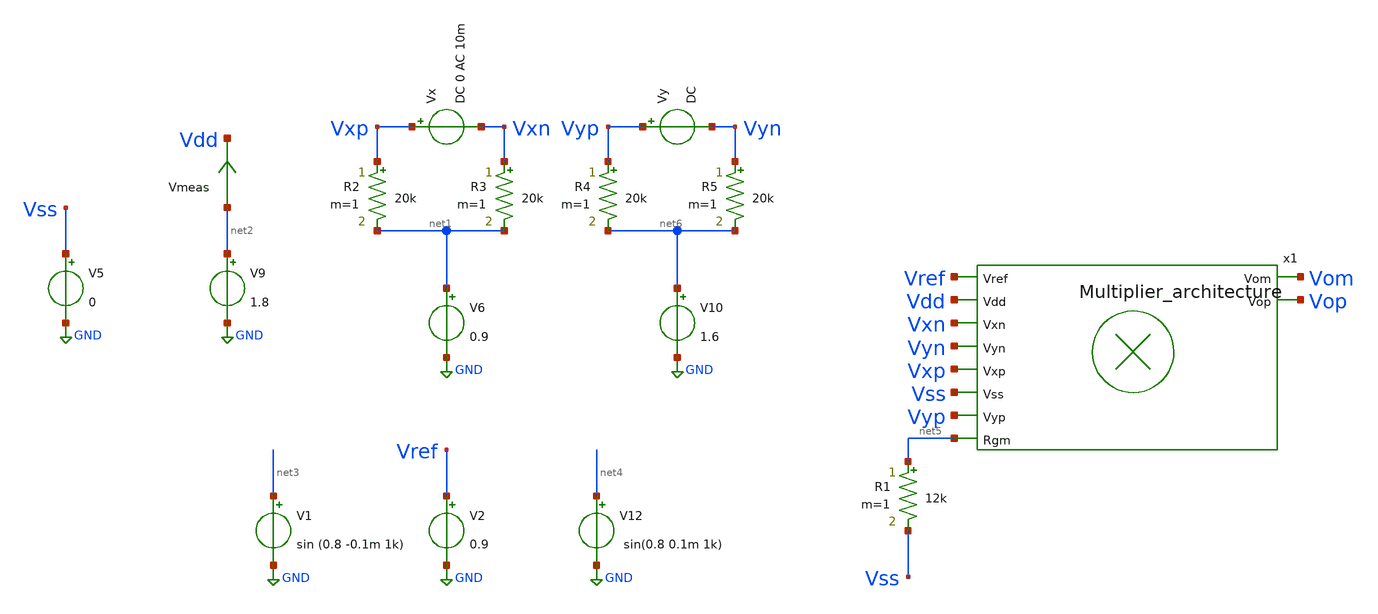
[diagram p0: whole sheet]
** sch_path: src/Multiplier/testbenches/Multiplier_tb.sch
**.subckt Multiplier_tb
x1 Vref Vom Vdd Vxn Vyn Vxp Vss Vyp Vop net5 Multiplier_architecture
Vx Vxp Vxn DC 0 AC 10m
V6 net1 GND 0.9
V9 net2 GND 1.8
Vmeas net2 Vdd 0
.save i(vmeas)
V1 net3 GND sin (0.8 -0.1m 1k)
V12 net4 GND sin(0.8 0.1m 1k)
V5 Vss GND 0
V2 Vref GND 0.9
R1 net5 Vss 12k m=1
R2 Vxp net1 20k m=1
R3 Vxn net1 20k m=1
Vy Vyp Vyn DC
V10 net6 GND 1.6
R4 Vyp net6 20k m=1
R5 Vyn net6 20k m=1
**** begin user architecture code

** opencircuitdesign pdks install
.lib $::SKYWATER_MODELS/sky130.lib.spice tt


**** end user architecture code
**.ends

* expanding   symbol:  /foss/designs/FYP/Sky130_Design/Multiplier/Src/Multiplier_architecture.sym #
*+ of pins=10
** sym_path: src/Multiplier/Src/Multiplier_architecture.sym
** sch_path: src/Multiplier/Src/Multiplier_architecture.sch
.subckt Multiplier_architecture Vref Vom Vdd Vxn Vyn Vxp Vss Vyp Vop Rgm
*.ipin Vxn
*.opin Vom
*.ipin Vxp
*.ipin Vyn
*.ipin Vyp
*.ipin Vref
*.ipin Vdd
*.ipin Vss
*.ipin Rgm
*.opin Vop
x1 Rgm Vom net1 Vdd Vref Vss Vop net2 Opamp_with_bias
XM1 Vxp Vyp net1 Vss sky130_fd_pr__nfet_01v8_lvt L=2 W=10 nf=1 ad='int((nf+1)/2) * W/nf * 0.29' as='int((nf+2)/2) * W/nf * 0.29'
+ pd='2*int((nf+1)/2) * (W/nf + 0.29)' ps='2*int((nf+2)/2) * (W/nf + 0.29)' nrd='0.29 / W' nrs='0.29 / W'
+ sa=0 sb=0 sd=0 mult=1 m=1
XM2 Vxp Vyn net2 Vss sky130_fd_pr__nfet_01v8_lvt L=2 W=10 nf=1 ad='int((nf+1)/2) * W/nf * 0.29' as='int((nf+2)/2) * W/nf * 0.29'
+ pd='2*int((nf+1)/2) * (W/nf + 0.29)' ps='2*int((nf+2)/2) * (W/nf + 0.29)' nrd='0.29 / W' nrs='0.29 / W'
+ sa=0 sb=0 sd=0 mult=1 m=1
XM3 Vxn Vyn net1 Vss sky130_fd_pr__nfet_01v8_lvt L=2 W=10 nf=1 ad='int((nf+1)/2) * W/nf * 0.29' as='int((nf+2)/2) * W/nf * 0.29'
+ pd='2*int((nf+1)/2) * (W/nf + 0.29)' ps='2*int((nf+2)/2) * (W/nf + 0.29)' nrd='0.29 / W' nrs='0.29 / W'
+ sa=0 sb=0 sd=0 mult=1 m=1
XM4 Vxn Vyp net2 Vss sky130_fd_pr__nfet_01v8_lvt L=2 W=10 nf=1 ad='int((nf+1)/2) * W/nf * 0.29' as='int((nf+2)/2) * W/nf * 0.29'
+ pd='2*int((nf+1)/2) * (W/nf + 0.29)' ps='2*int((nf+2)/2) * (W/nf + 0.29)' nrd='0.29 / W' nrs='0.29 / W'
+ sa=0 sb=0 sd=0 mult=1 m=1
R1 net1 Vom 20k m=1
R2 net2 Vop 20k m=1
.ends


* expanding   symbol:  /foss/designs/FYP/Sky130_Design/Opamp_Design/src/Opamp_with_bias.sym # of
*+ pins=8
** sym_path: src/Opamp_Design/src/Opamp_with_bias.sym
** sch_path: src/Opamp_Design/src/Opamp_with_bias.sch
.subckt Opamp_with_bias Rgm Vop Vm Vdd Vref Vss Vom Vp
*.ipin Vdd
*.ipin Vss
*.opin Vop
*.opin Vom
*.ipin Vm
*.ipin Vp
*.ipin Vref
*.ipin Rgm
XM32 NBias PBias Vdd Vdd sky130_fd_pr__pfet_01v8_lvt L=1 W=5 nf=1 ad='int((nf+1)/2) * W/nf * 0.29' as='int((nf+2)/2) * W/nf * 0.29'
+ pd='2*int((nf+1)/2) * (W/nf + 0.29)' ps='2*int((nf+2)/2) * (W/nf + 0.29)' nrd='0.29 / W' nrs='0.29 / W'
+ sa=0 sb=0 sd=0 mult=2 m=2
XM33 NBias NBias Vss Vss sky130_fd_pr__nfet_01v8_lvt L=2 W=5 nf=1 ad='int((nf+1)/2) * W/nf * 0.29' as='int((nf+2)/2) * W/nf * 0.29'
+ pd='2*int((nf+1)/2) * (W/nf + 0.29)' ps='2*int((nf+2)/2) * (W/nf + 0.29)' nrd='0.29 / W' nrs='0.29 / W'
+ sa=0 sb=0 sd=0 mult=2 m=2
XM34 net1 PBias Vdd Vdd sky130_fd_pr__pfet_01v8_lvt L=1 W=5 nf=1 ad='int((nf+1)/2) * W/nf * 0.29' as='int((nf+2)/2) * W/nf * 0.29'
+ pd='2*int((nf+1)/2) * (W/nf + 0.29)' ps='2*int((nf+2)/2) * (W/nf + 0.29)' nrd='0.29 / W' nrs='0.29 / W'
+ sa=0 sb=0 sd=0 mult=2 m=2
XM35 net1 net1 Rgm Vss sky130_fd_pr__nfet_01v8_lvt L=1 W=10 nf=1 ad='int((nf+1)/2) * W/nf * 0.29' as='int((nf+2)/2) * W/nf * 0.29'
+ pd='2*int((nf+1)/2) * (W/nf + 0.29)' ps='2*int((nf+2)/2) * (W/nf + 0.29)' nrd='0.29 / W' nrs='0.29 / W'
+ sa=0 sb=0 sd=0 mult=2 m=2
XM36 net2 net1 Vss Vss sky130_fd_pr__nfet_01v8_lvt L=2 W=5 nf=1 ad='int((nf+1)/2) * W/nf * 0.29' as='int((nf+2)/2) * W/nf * 0.29'
+ pd='2*int((nf+1)/2) * (W/nf + 0.29)' ps='2*int((nf+2)/2) * (W/nf + 0.29)' nrd='0.29 / W' nrs='0.29 / W'
+ sa=0 sb=0 sd=0 mult=2 m=2
XM37 PBias NBias Vss Vss sky130_fd_pr__nfet_01v8_lvt L=2 W=5 nf=1 ad='int((nf+1)/2) * W/nf * 0.29' as='int((nf+2)/2) * W/nf * 0.29'
+ pd='2*int((nf+1)/2) * (W/nf + 0.29)' ps='2*int((nf+2)/2) * (W/nf + 0.29)' nrd='0.29 / W' nrs='0.29 / W'
+ sa=0 sb=0 sd=0 mult=2 m=2
XM38 PBias net2 Vdd Vdd sky130_fd_pr__pfet_01v8_lvt L=1 W=5 nf=1 ad='int((nf+1)/2) * W/nf * 0.29' as='int((nf+2)/2) * W/nf * 0.29'
+ pd='2*int((nf+1)/2) * (W/nf + 0.29)' ps='2*int((nf+2)/2) * (W/nf + 0.29)' nrd='0.29 / W' nrs='0.29 / W'
+ sa=0 sb=0 sd=0 mult=2 m=2
XM39 net2 net2 Vdd Vdd sky130_fd_pr__pfet_01v8_lvt L=1 W=5 nf=1 ad='int((nf+1)/2) * W/nf * 0.29' as='int((nf+2)/2) * W/nf * 0.29'
+ pd='2*int((nf+1)/2) * (W/nf + 0.29)' ps='2*int((nf+2)/2) * (W/nf + 0.29)' nrd='0.29 / W' nrs='0.29 / W'
+ sa=0 sb=0 sd=0 mult=2 m=2
XM40 PBias net3 NBias Vss sky130_fd_pr__nfet_01v8_lvt L=1 W=2 nf=1 ad='int((nf+1)/2) * W/nf * 0.29' as='int((nf+2)/2) * W/nf * 0.29'
+ pd='2*int((nf+1)/2) * (W/nf + 0.29)' ps='2*int((nf+2)/2) * (W/nf + 0.29)' nrd='0.29 / W' nrs='0.29 / W'
+ sa=0 sb=0 sd=0 mult=1 m=1
XM41 net3 NBias Vss Vss sky130_fd_pr__nfet_01v8_lvt L=2 W=5 nf=1 ad='int((nf+1)/2) * W/nf * 0.29' as='int((nf+2)/2) * W/nf * 0.29'
+ pd='2*int((nf+1)/2) * (W/nf + 0.29)' ps='2*int((nf+2)/2) * (W/nf + 0.29)' nrd='0.29 / W' nrs='0.29 / W'
+ sa=0 sb=0 sd=0 mult=2 m=2
XM42 net3 net3 Vdd Vdd sky130_fd_pr__pfet_01v8_lvt L=20 W=1 nf=1 ad='int((nf+1)/2) * W/nf * 0.29' as='int((nf+2)/2) * W/nf * 0.29'
+ pd='2*int((nf+1)/2) * (W/nf + 0.29)' ps='2*int((nf+2)/2) * (W/nf + 0.29)' nrd='0.29 / W' nrs='0.29 / W'
+ sa=0 sb=0 sd=0 mult=2 m=2
XM43 net4 PBias Vdd Vdd sky130_fd_pr__pfet_01v8_lvt L=1 W=5 nf=1 ad='int((nf+1)/2) * W/nf * 0.29' as='int((nf+2)/2) * W/nf * 0.29'
+ pd='2*int((nf+1)/2) * (W/nf + 0.29)' ps='2*int((nf+2)/2) * (W/nf + 0.29)' nrd='0.29 / W' nrs='0.29 / W'
+ sa=0 sb=0 sd=0 mult=2 m=2
XM44 net5 PBias Vdd Vdd sky130_fd_pr__pfet_01v8_lvt L=1 W=5 nf=1 ad='int((nf+1)/2) * W/nf * 0.29' as='int((nf+2)/2) * W/nf * 0.29'
+ pd='2*int((nf+1)/2) * (W/nf + 0.29)' ps='2*int((nf+2)/2) * (W/nf + 0.29)' nrd='0.29 / W' nrs='0.29 / W'
+ sa=0 sb=0 sd=0 mult=2 m=2
XM45 net6 PBias Vdd Vdd sky130_fd_pr__pfet_01v8_lvt L=1 W=5 nf=1 ad='int((nf+1)/2) * W/nf * 0.29' as='int((nf+2)/2) * W/nf * 0.29'
+ pd='2*int((nf+1)/2) * (W/nf + 0.29)' ps='2*int((nf+2)/2) * (W/nf + 0.29)' nrd='0.29 / W' nrs='0.29 / W'
+ sa=0 sb=0 sd=0 mult=2 m=2
XM54 net7 PBias Vdd Vdd sky130_fd_pr__pfet_01v8_lvt L=1 W=5 nf=1 ad='int((nf+1)/2) * W/nf * 0.29' as='int((nf+2)/2) * W/nf * 0.29'
+ pd='2*int((nf+1)/2) * (W/nf + 0.29)' ps='2*int((nf+2)/2) * (W/nf + 0.29)' nrd='0.29 / W' nrs='0.29 / W'
+ sa=0 sb=0 sd=0 mult=2 m=2
XC1 Vop1 Vom sky130_fd_pr__cap_mim_m3_1 W=10 L=10 MF=5 m=5
XC2 Vom1 Vop sky130_fd_pr__cap_mim_m3_1 W=10 L=10 MF=5 m=5
x1 net6 net5 net4 Vm Vp Vss Vdd Vref Vop1 Vom1 Diff_opamp
x2 Vref net7 Vop1 Vom1 Vss Vdd Vop Vom Common_source_stage
.ends


* expanding   symbol:  /foss/designs/FYP/Sky130_Design/Opamp_Design/src/Diff_opamp.sym # of pins=10
** sym_path: src/Opamp_Design/src/Diff_opamp.sym
** sch_path: src/Opamp_Design/src/Diff_opamp.sch
.subckt Diff_opamp Vbias3 Vbias2 Vbias1 Vm Vp Vss Vdd Vref Vop Vom
*.ipin Vss
*.opin Vop
*.ipin Vdd
*.ipin Vp
*.ipin Vm
*.ipin Vref
*.opin Vom
*.ipin Vbias1
*.ipin Vbias2
*.ipin Vbias3
XM5 Vtest2 Vm net2 Vss sky130_fd_pr__nfet_01v8_lvt L=4 W=4 nf=1 ad='int((nf+1)/2) * W/nf * 0.29' as='int((nf+2)/2) * W/nf * 0.29'
+ pd='2*int((nf+1)/2) * (W/nf + 0.29)' ps='2*int((nf+2)/2) * (W/nf + 0.29)' nrd='0.29 / W' nrs='0.29 / W'
+ sa=0 sb=0 sd=0 mult=2 m=2
XM6 net1 Vp net2 Vss sky130_fd_pr__nfet_01v8_lvt L=4 W=4 nf=1 ad='int((nf+1)/2) * W/nf * 0.29' as='int((nf+2)/2) * W/nf * 0.29'
+ pd='2*int((nf+1)/2) * (W/nf + 0.29)' ps='2*int((nf+2)/2) * (W/nf + 0.29)' nrd='0.29 / W' nrs='0.29 / W'
+ sa=0 sb=0 sd=0 mult=2 m=2
XM11 Vop Vbias Vtest2 Vdd sky130_fd_pr__pfet_01v8_lvt L=5 W=2 nf=1 ad='int((nf+1)/2) * W/nf * 0.29' as='int((nf+2)/2) * W/nf * 0.29'
+ pd='2*int((nf+1)/2) * (W/nf + 0.29)' ps='2*int((nf+2)/2) * (W/nf + 0.29)' nrd='0.29 / W' nrs='0.29 / W'
+ sa=0 sb=0 sd=0 mult=2 m=2
XM12 Vom Vbias net1 Vdd sky130_fd_pr__pfet_01v8_lvt L=5 W=2 nf=1 ad='int((nf+1)/2) * W/nf * 0.29' as='int((nf+2)/2) * W/nf * 0.29'
+ pd='2*int((nf+1)/2) * (W/nf + 0.29)' ps='2*int((nf+2)/2) * (W/nf + 0.29)' nrd='0.29 / W' nrs='0.29 / W'
+ sa=0 sb=0 sd=0 mult=2 m=2
XM13 Vtest2 Vout Vdd Vdd sky130_fd_pr__pfet_01v8_lvt L=5 W=2 nf=1 ad='int((nf+1)/2) * W/nf * 0.29' as='int((nf+2)/2) * W/nf * 0.29'
+ pd='2*int((nf+1)/2) * (W/nf + 0.29)' ps='2*int((nf+2)/2) * (W/nf + 0.29)' nrd='0.29 / W' nrs='0.29 / W'
+ sa=0 sb=0 sd=0 mult=4 m=4
XM14 net1 Vout Vdd Vdd sky130_fd_pr__pfet_01v8_lvt L=5 W=2 nf=1 ad='int((nf+1)/2) * W/nf * 0.29' as='int((nf+2)/2) * W/nf * 0.29'
+ pd='2*int((nf+1)/2) * (W/nf + 0.29)' ps='2*int((nf+2)/2) * (W/nf + 0.29)' nrd='0.29 / W' nrs='0.29 / W'
+ sa=0 sb=0 sd=0 mult=4 m=4
XM19 net2 Vbias2 net3 Vss sky130_fd_pr__nfet_01v8_lvt L=1 W=1 nf=1 ad='int((nf+1)/2) * W/nf * 0.29' as='int((nf+2)/2) * W/nf * 0.29'
+ pd='2*int((nf+1)/2) * (W/nf + 0.29)' ps='2*int((nf+2)/2) * (W/nf + 0.29)' nrd='0.29 / W' nrs='0.29 / W'
+ sa=0 sb=0 sd=0 mult=2 m=2
XM1 net3 Vbias1 Vss Vss sky130_fd_pr__nfet_01v8_lvt L=10 W=1 nf=1 ad='int((nf+1)/2) * W/nf * 0.29' as='int((nf+2)/2) * W/nf * 0.29'
+ pd='2*int((nf+1)/2) * (W/nf + 0.29)' ps='2*int((nf+2)/2) * (W/nf + 0.29)' nrd='0.29 / W' nrs='0.29 / W'
+ sa=0 sb=0 sd=0 mult=2 m=2
XM2 net4 Vbias1 Vss Vss sky130_fd_pr__nfet_01v8_lvt L=10 W=1 nf=1 ad='int((nf+1)/2) * W/nf * 0.29' as='int((nf+2)/2) * W/nf * 0.29'
+ pd='2*int((nf+1)/2) * (W/nf + 0.29)' ps='2*int((nf+2)/2) * (W/nf + 0.29)' nrd='0.29 / W' nrs='0.29 / W'
+ sa=0 sb=0 sd=0 mult=2 m=2
XM3 net2 Vbias2 net4 Vss sky130_fd_pr__nfet_01v8_lvt L=1 W=1 nf=1 ad='int((nf+1)/2) * W/nf * 0.29' as='int((nf+2)/2) * W/nf * 0.29'
+ pd='2*int((nf+1)/2) * (W/nf + 0.29)' ps='2*int((nf+2)/2) * (W/nf + 0.29)' nrd='0.29 / W' nrs='0.29 / W'
+ sa=0 sb=0 sd=0 mult=2 m=2
XM4 Vop Vbias2 net5 Vss sky130_fd_pr__nfet_01v8_lvt L=1 W=1 nf=1 ad='int((nf+1)/2) * W/nf * 0.29' as='int((nf+2)/2) * W/nf * 0.29'
+ pd='2*int((nf+1)/2) * (W/nf + 0.29)' ps='2*int((nf+2)/2) * (W/nf + 0.29)' nrd='0.29 / W' nrs='0.29 / W'
+ sa=0 sb=0 sd=0 mult=2 m=2
XM7 net5 Vbias1 Vss Vss sky130_fd_pr__nfet_01v8_lvt L=10 W=1 nf=1 ad='int((nf+1)/2) * W/nf * 0.29' as='int((nf+2)/2) * W/nf * 0.29'
+ pd='2*int((nf+1)/2) * (W/nf + 0.29)' ps='2*int((nf+2)/2) * (W/nf + 0.29)' nrd='0.29 / W' nrs='0.29 / W'
+ sa=0 sb=0 sd=0 mult=2 m=2
XM8 Vom Vbias2 net6 Vss sky130_fd_pr__nfet_01v8_lvt L=1 W=1 nf=1 ad='int((nf+1)/2) * W/nf * 0.29' as='int((nf+2)/2) * W/nf * 0.29'
+ pd='2*int((nf+1)/2) * (W/nf + 0.29)' ps='2*int((nf+2)/2) * (W/nf + 0.29)' nrd='0.29 / W' nrs='0.29 / W'
+ sa=0 sb=0 sd=0 mult=2 m=2
XM9 net6 Vbias1 Vss Vss sky130_fd_pr__nfet_01v8_lvt L=10 W=1 nf=1 ad='int((nf+1)/2) * W/nf * 0.29' as='int((nf+2)/2) * W/nf * 0.29'
+ pd='2*int((nf+1)/2) * (W/nf + 0.29)' ps='2*int((nf+2)/2) * (W/nf + 0.29)' nrd='0.29 / W' nrs='0.29 / W'
+ sa=0 sb=0 sd=0 mult=2 m=2
XM10 Vout Vref net8 Vss sky130_fd_pr__nfet_01v8_lvt L=20 W=5 nf=1 ad='int((nf+1)/2) * W/nf * 0.29' as='int((nf+2)/2) * W/nf * 0.29'
+ pd='2*int((nf+1)/2) * (W/nf + 0.29)' ps='2*int((nf+2)/2) * (W/nf + 0.29)' nrd='0.29 / W' nrs='0.29 / W'
+ sa=0 sb=0 sd=0 mult=2 m=2
XM17 net9 Vop net8 Vss sky130_fd_pr__nfet_01v8_lvt L=20 W=5 nf=1 ad='int((nf+1)/2) * W/nf * 0.29' as='int((nf+2)/2) * W/nf * 0.29'
+ pd='2*int((nf+1)/2) * (W/nf + 0.29)' ps='2*int((nf+2)/2) * (W/nf + 0.29)' nrd='0.29 / W' nrs='0.29 / W'
+ sa=0 sb=0 sd=0 mult=2 m=2
XM18 net9 Vom net7 Vss sky130_fd_pr__nfet_01v8_lvt L=20 W=5 nf=1 ad='int((nf+1)/2) * W/nf * 0.29' as='int((nf+2)/2) * W/nf * 0.29'
+ pd='2*int((nf+1)/2) * (W/nf + 0.29)' ps='2*int((nf+2)/2) * (W/nf + 0.29)' nrd='0.29 / W' nrs='0.29 / W'
+ sa=0 sb=0 sd=0 mult=2 m=2
XM22 net7 Vbias1 Vss Vss sky130_fd_pr__nfet_01v8_lvt L=20 W=1 nf=1 ad='int((nf+1)/2) * W/nf * 0.29' as='int((nf+2)/2) * W/nf * 0.29'
+ pd='2*int((nf+1)/2) * (W/nf + 0.29)' ps='2*int((nf+2)/2) * (W/nf + 0.29)' nrd='0.29 / W' nrs='0.29 / W'
+ sa=0 sb=0 sd=0 mult=2 m=2
XM20 net9 net9 Vdd Vdd sky130_fd_pr__pfet_01v8_lvt L=10 W=1 nf=1 ad='int((nf+1)/2) * W/nf * 0.29' as='int((nf+2)/2) * W/nf * 0.29'
+ pd='2*int((nf+1)/2) * (W/nf + 0.29)' ps='2*int((nf+2)/2) * (W/nf + 0.29)' nrd='0.29 / W' nrs='0.29 / W'
+ sa=0 sb=0 sd=0 mult=2 m=2
XM21 Vout net9 Vdd Vdd sky130_fd_pr__pfet_01v8_lvt L=10 W=1 nf=1 ad='int((nf+1)/2) * W/nf * 0.29' as='int((nf+2)/2) * W/nf * 0.29'
+ pd='2*int((nf+1)/2) * (W/nf + 0.29)' ps='2*int((nf+2)/2) * (W/nf + 0.29)' nrd='0.29 / W' nrs='0.29 / W'
+ sa=0 sb=0 sd=0 mult=2 m=2
XM15 net8 Vbias1 Vss Vss sky130_fd_pr__nfet_01v8_lvt L=20 W=1 nf=1 ad='int((nf+1)/2) * W/nf * 0.29' as='int((nf+2)/2) * W/nf * 0.29'
+ pd='2*int((nf+1)/2) * (W/nf + 0.29)' ps='2*int((nf+2)/2) * (W/nf + 0.29)' nrd='0.29 / W' nrs='0.29 / W'
+ sa=0 sb=0 sd=0 mult=2 m=2
XM16 Vout Vref net7 Vss sky130_fd_pr__nfet_01v8_lvt L=20 W=5 nf=1 ad='int((nf+1)/2) * W/nf * 0.29' as='int((nf+2)/2) * W/nf * 0.29'
+ pd='2*int((nf+1)/2) * (W/nf + 0.29)' ps='2*int((nf+2)/2) * (W/nf + 0.29)' nrd='0.29 / W' nrs='0.29 / W'
+ sa=0 sb=0 sd=0 mult=2 m=2
XM46 Vbias1 Vbias1 Vss Vss sky130_fd_pr__nfet_01v8_lvt L=2 W=1 nf=1 ad='int((nf+1)/2) * W/nf * 0.29'
+ as='int((nf+2)/2) * W/nf * 0.29' pd='2*int((nf+1)/2) * (W/nf + 0.29)' ps='2*int((nf+2)/2) * (W/nf + 0.29)'
+ nrd='0.29 / W' nrs='0.29 / W' sa=0 sb=0 sd=0 mult=2 m=2
XM47 Vbias2 Vbias2 Vss Vss sky130_fd_pr__nfet_01v8_lvt L=5 W=0.6 nf=1 ad='int((nf+1)/2) * W/nf * 0.29'
+ as='int((nf+2)/2) * W/nf * 0.29' pd='2*int((nf+1)/2) * (W/nf + 0.29)' ps='2*int((nf+2)/2) * (W/nf + 0.29)'
+ nrd='0.29 / W' nrs='0.29 / W' sa=0 sb=0 sd=0 mult=2 m=2
XM23 Vbias3 Vbias3 Vss Vss sky130_fd_pr__nfet_01v8_lvt L=1 W=0.6 nf=1 ad='int((nf+1)/2) * W/nf * 0.29'
+ as='int((nf+2)/2) * W/nf * 0.29' pd='2*int((nf+1)/2) * (W/nf + 0.29)' ps='2*int((nf+2)/2) * (W/nf + 0.29)'
+ nrd='0.29 / W' nrs='0.29 / W' sa=0 sb=0 sd=0 mult=2 m=2
XM24 Vbias Vbias3 Vss Vss sky130_fd_pr__nfet_01v8_lvt L=1 W=0.6 nf=1 ad='int((nf+1)/2) * W/nf * 0.29'
+ as='int((nf+2)/2) * W/nf * 0.29' pd='2*int((nf+1)/2) * (W/nf + 0.29)' ps='2*int((nf+2)/2) * (W/nf + 0.29)'
+ nrd='0.29 / W' nrs='0.29 / W' sa=0 sb=0 sd=0 mult=2 m=2
XM25 Vbias Vbias Vdd Vdd sky130_fd_pr__pfet_01v8_lvt L=10 W=1.5 nf=1 ad='int((nf+1)/2) * W/nf * 0.29'
+ as='int((nf+2)/2) * W/nf * 0.29' pd='2*int((nf+1)/2) * (W/nf + 0.29)' ps='2*int((nf+2)/2) * (W/nf + 0.29)'
+ nrd='0.29 / W' nrs='0.29 / W' sa=0 sb=0 sd=0 mult=2 m=2
.ends


* expanding   symbol:  /foss/designs/FYP/Sky130_Design/Opamp_Design/src/Common_source_stage.sym # of
*+ pins=8
** sym_path: src/Opamp_Design/src/Common_source_stage.sym
** sch_path: src/Opamp_Design/src/Common_source_stage.sch
.subckt Common_source_stage Vref Vbias Vomin Vopin Vss Vdd Vop Vom
*.ipin Vdd
*.opin Vop
*.ipin Vss
*.opin Vom
*.ipin Vopin
*.ipin Vomin
*.ipin Vbias
*.ipin Vref
XM9 Vop Vopin Vdd Vdd sky130_fd_pr__pfet_01v8_lvt L=1 W=2 nf=1 ad='int((nf+1)/2) * W/nf * 0.29' as='int((nf+2)/2) * W/nf * 0.29'
+ pd='2*int((nf+1)/2) * (W/nf + 0.29)' ps='2*int((nf+2)/2) * (W/nf + 0.29)' nrd='0.29 / W' nrs='0.29 / W'
+ sa=0 sb=0 sd=0 mult=9 m=9
XM4 Vom Vomin Vdd Vdd sky130_fd_pr__pfet_01v8_lvt L=1 W=2 nf=1 ad='int((nf+1)/2) * W/nf * 0.29' as='int((nf+2)/2) * W/nf * 0.29'
+ pd='2*int((nf+1)/2) * (W/nf + 0.29)' ps='2*int((nf+2)/2) * (W/nf + 0.29)' nrd='0.29 / W' nrs='0.29 / W'
+ sa=0 sb=0 sd=0 mult=9 m=9
XM2 Vop Vout Vss Vss sky130_fd_pr__nfet_01v8_lvt L=1 W=1 nf=1 ad='int((nf+1)/2) * W/nf * 0.29' as='int((nf+2)/2) * W/nf * 0.29'
+ pd='2*int((nf+1)/2) * (W/nf + 0.29)' ps='2*int((nf+2)/2) * (W/nf + 0.29)' nrd='0.29 / W' nrs='0.29 / W'
+ sa=0 sb=0 sd=0 mult=9 m=9
XM1 Vom Vout Vss Vss sky130_fd_pr__nfet_01v8_lvt L=1 W=1 nf=1 ad='int((nf+1)/2) * W/nf * 0.29' as='int((nf+2)/2) * W/nf * 0.29'
+ pd='2*int((nf+1)/2) * (W/nf + 0.29)' ps='2*int((nf+2)/2) * (W/nf + 0.29)' nrd='0.29 / W' nrs='0.29 / W'
+ sa=0 sb=0 sd=0 mult=9 m=9
XM3 net1 Vbiasp Vdd Vdd sky130_fd_pr__pfet_01v8_lvt L=5 W=1 nf=1 ad='int((nf+1)/2) * W/nf * 0.29' as='int((nf+2)/2) * W/nf * 0.29'
+ pd='2*int((nf+1)/2) * (W/nf + 0.29)' ps='2*int((nf+2)/2) * (W/nf + 0.29)' nrd='0.29 / W' nrs='0.29 / W'
+ sa=0 sb=0 sd=0 mult=2 m=2
XM7 Vtest Vcm net1 Vdd sky130_fd_pr__pfet_01v8_lvt L=10 W=1 nf=1 ad='int((nf+1)/2) * W/nf * 0.29' as='int((nf+2)/2) * W/nf * 0.29'
+ pd='2*int((nf+1)/2) * (W/nf + 0.29)' ps='2*int((nf+2)/2) * (W/nf + 0.29)' nrd='0.29 / W' nrs='0.29 / W'
+ sa=0 sb=0 sd=0 mult=2 m=2
XM8 Vout Vref net1 Vdd sky130_fd_pr__pfet_01v8_lvt L=10 W=1 nf=1 ad='int((nf+1)/2) * W/nf * 0.29' as='int((nf+2)/2) * W/nf * 0.29'
+ pd='2*int((nf+1)/2) * (W/nf + 0.29)' ps='2*int((nf+2)/2) * (W/nf + 0.29)' nrd='0.29 / W' nrs='0.29 / W'
+ sa=0 sb=0 sd=0 mult=2 m=2
XM5 Vtest Vtest Vss Vss sky130_fd_pr__nfet_01v8_lvt L=20 W=0.5 nf=1 ad='int((nf+1)/2) * W/nf * 0.29'
+ as='int((nf+2)/2) * W/nf * 0.29' pd='2*int((nf+1)/2) * (W/nf + 0.29)' ps='2*int((nf+2)/2) * (W/nf + 0.29)'
+ nrd='0.29 / W' nrs='0.29 / W' sa=0 sb=0 sd=0 mult=2 m=2
XM6 Vout Vtest Vss Vss sky130_fd_pr__nfet_01v8_lvt L=20 W=0.5 nf=1 ad='int((nf+1)/2) * W/nf * 0.29' as='int((nf+2)/2) * W/nf * 0.29'
+ pd='2*int((nf+1)/2) * (W/nf + 0.29)' ps='2*int((nf+2)/2) * (W/nf + 0.29)' nrd='0.29 / W' nrs='0.29 / W'
+ sa=0 sb=0 sd=0 mult=2 m=2
x1 Vop Vcm res_pack
x2 Vcm Vom res_pack
XM10 Vbias Vbias Vss Vss sky130_fd_pr__nfet_01v8_lvt L=1 W=0.6 nf=1 ad='int((nf+1)/2) * W/nf * 0.29'
+ as='int((nf+2)/2) * W/nf * 0.29' pd='2*int((nf+1)/2) * (W/nf + 0.29)' ps='2*int((nf+2)/2) * (W/nf + 0.29)'
+ nrd='0.29 / W' nrs='0.29 / W' sa=0 sb=0 sd=0 mult=2 m=2
XM11 Vbiasp Vbias Vss Vss sky130_fd_pr__nfet_01v8_lvt L=1 W=0.6 nf=1 ad='int((nf+1)/2) * W/nf * 0.29'
+ as='int((nf+2)/2) * W/nf * 0.29' pd='2*int((nf+1)/2) * (W/nf + 0.29)' ps='2*int((nf+2)/2) * (W/nf + 0.29)'
+ nrd='0.29 / W' nrs='0.29 / W' sa=0 sb=0 sd=0 mult=2 m=2
XM12 Vbiasp Vbiasp Vdd Vdd sky130_fd_pr__pfet_01v8_lvt L=1 W=6 nf=1 ad='int((nf+1)/2) * W/nf * 0.29'
+ as='int((nf+2)/2) * W/nf * 0.29' pd='2*int((nf+1)/2) * (W/nf + 0.29)' ps='2*int((nf+2)/2) * (W/nf + 0.29)'
+ nrd='0.29 / W' nrs='0.29 / W' sa=0 sb=0 sd=0 mult=2 m=2
.ends


* expanding   symbol:  /foss/designs/FYP/Sky130_Design/Opamp_Design/src/res_pack.sym # of pins=2
** sym_path: src/Opamp_Design/src/res_pack.sym
** sch_path: src/Opamp_Design/src/res_pack.sch
.subckt res_pack Vin Vout
*.ipin Vin
*.opin Vout
XR1 net4 Vin sky130_fd_pr__res_generic_po W=0.5 L=40 m=1
XR2 net5 net4 sky130_fd_pr__res_generic_po W=0.5 L=40 m=1
XR3 net6 net5 sky130_fd_pr__res_generic_po W=0.5 L=40 m=1
XR4 net7 net6 sky130_fd_pr__res_generic_po W=0.5 L=40 m=1
XR5 net1 net7 sky130_fd_pr__res_generic_po W=0.5 L=40 m=1
XR6 net8 net2 sky130_fd_pr__res_generic_po W=0.5 L=40 m=1
XR7 net9 net8 sky130_fd_pr__res_generic_po W=0.5 L=40 m=1
XR8 net10 net9 sky130_fd_pr__res_generic_po W=0.5 L=40 m=1
XR9 net11 net10 sky130_fd_pr__res_generic_po W=0.5 L=40 m=1
XR10 net1 net11 sky130_fd_pr__res_generic_po W=0.5 L=40 m=1
XR11 net12 net2 sky130_fd_pr__res_generic_po W=0.5 L=40 m=1
XR12 net13 net12 sky130_fd_pr__res_generic_po W=0.5 L=40 m=1
XR13 net14 net13 sky130_fd_pr__res_generic_po W=0.5 L=40 m=1
XR14 net15 net14 sky130_fd_pr__res_generic_po W=0.5 L=40 m=1
XR16 net16 Vout sky130_fd_pr__res_generic_po W=0.5 L=40 m=1
XR17 net17 net16 sky130_fd_pr__res_generic_po W=0.5 L=40 m=1
XR18 net18 net17 sky130_fd_pr__res_generic_po W=0.5 L=40 m=1
XR19 net19 net18 sky130_fd_pr__res_generic_po W=0.5 L=40 m=1
XR20 net3 net19 sky130_fd_pr__res_generic_po W=0.5 L=40 m=1
XR15 net3 net15 sky130_fd_pr__res_generic_po W=0.5 L=40 m=1
.ends

.GLOBAL GND
**** begin user architecture code



* ngspice commands
.options savecurrents

.control
save all
save @m.x1.x1.x2.x1.xm5.msky130_fd_pr__nfet_01v8_lvt[gm]
save @m.x1.x1.x2.x1.xm1.msky130_fd_pr__nfet_01v8_lvt[gm]
save @m.x1.x1.x2.x1.xm2.msky130_fd_pr__nfet_01v8_lvt[gm]
save @m.x1.x1.x2.x1.xm3.msky130_fd_pr__nfet_01v8_lvt[gm]
save @m.x1.x1.x2.x1.xm4.msky130_fd_pr__nfet_01v8_lvt[gm]
save @m.x1.x1.x2.x1.xm6.msky130_fd_pr__nfet_01v8_lvt[gm]
save @m.x1.x1.x2.x1.xm7.msky130_fd_pr__nfet_01v8_lvt[gm]
save @m.x1.x1.x2.x1.xm8.msky130_fd_pr__nfet_01v8_lvt[gm]
save @m.x1.x1.x2.x1.xm9.msky130_fd_pr__nfet_01v8_lvt[gm]
save @m.x1.x1.x2.x1.xm10.msky130_fd_pr__nfet_01v8_lvt[gm]
save @m.x1.x1.x2.x1.xm11.msky130_fd_pr__pfet_01v8_lvt[gm]
save @m.x1.x1.x2.x1.xm12.msky130_fd_pr__pfet_01v8_lvt[gm]
save @m.x1.x1.x2.x1.xm13.msky130_fd_pr__pfet_01v8_lvt[gm]
save @m.x1.x1.x2.x1.xm14.msky130_fd_pr__pfet_01v8_lvt[gm]
save @m.x1.x1.x2.x1.xm15.msky130_fd_pr__nfet_01v8_lvt[gm]
save @m.x1.x1.x2.x1.xm16.msky130_fd_pr__nfet_01v8_lvt[gm]
save @m.x1.x1.x2.x1.xm17.msky130_fd_pr__nfet_01v8_lvt[gm]
save @m.x1.x1.x2.x1.xm18.msky130_fd_pr__nfet_01v8_lvt[gm]
save @m.x1.x1.x2.x1.xm19.msky130_fd_pr__nfet_01v8_lvt[gm]
save @m.x1.x1.x2.x1.xm20.msky130_fd_pr__pfet_01v8_lvt[gm]
save @m.x1.x1.x2.x1.xm21.msky130_fd_pr__pfet_01v8_lvt[gm]
save @m.x1.x1.x2.x1.xm22.msky130_fd_pr__nfet_01v8_lvt[gm]

save @m.x1.x1.x2.x2.xm1.msky130_fd_pr__nfet_01v8_lvt[gm]
save @m.x1.x1.x2.x2.xm2.msky130_fd_pr__nfet_01v8_lvt[gm]
save @m.x1.x1.x2.x2.xm3.msky130_fd_pr__pfet_01v8_lvt[gm]
save @m.x1.x1.x2.x2.xm4.msky130_fd_pr__pfet_01v8_lvt[gm]
save @m.x1.x1.x2.x2.xm5.msky130_fd_pr__nfet_01v8_lvt[gm]
save @m.x1.x1.x2.x2.xm6.msky130_fd_pr__nfet_01v8_lvt[gm]
save @m.x1.x1.x2.x2.xm7.msky130_fd_pr__pfet_01v8_lvt[gm]
save @m.x1.x1.x2.x2.xm8.msky130_fd_pr__pfet_01v8_lvt[gm]
save @m.x1.x1.x2.x2.xm9.msky130_fd_pr__pfet_01v8_lvt[gm]

save @m.x1.x1.x1.xm5.msky130_fd_pr__pfet_01v8_lvt[gm]
save @m.x1.x1.x1.xm1.msky130_fd_pr__pfet_01v8_lvt[gm]
save @m.x1.x1.x1.xm2.msky130_fd_pr__nfet_01v8_lvt[gm]
save @m.x1.x1.x1.xm3.msky130_fd_pr__nfet_01v8_lvt[gm]
save @m.x1.x1.x1.xm4.msky130_fd_pr__nfet_01v8_lvt[gm]
save @m.x1.x1.x1.xm6.msky130_fd_pr__pfet_01v8_lvt[gm]
save @m.x1.x1.x1.xm7.msky130_fd_pr__pfet_01v8_lvt[gm]
save @m.x1.x1.x1.xm8.msky130_fd_pr__pfet_01v8_lvt[gm]
save @m.x1.x1.x1.xm9.msky130_fd_pr__nfet_01v8_lvt[gm]
save @m.x1.x1.x1.xm10.msky130_fd_pr__nfet_01v8_lvt[gm]
save @m.x1.x1.x1.xm11.msky130_fd_pr__pfet_01v8_lvt[gm]
save @m.x1.x1.x1.xm12.msky130_fd_pr__nfet_01v8_lvt[gm]
save @m.x1.x1.x1.xm13.msky130_fd_pr__nfet_01v8_lvt[gm]
save @m.x1.x1.x1.xm14.msky130_fd_pr__nfet_01v8_lvt[gm]
save @m.x1.x1.x1.xm15.msky130_fd_pr__nfet_01v8_lvt[gm]
save @m.x1.x1.x1.xm16.msky130_fd_pr__pfet_01v8_lvt[gm]
save @m.x1.x1.x1.xm17.msky130_fd_pr__pfet_01v8_lvt[gm]
save @m.x1.x1.x1.xm18.msky130_fd_pr__pfet_01v8_lvt[gm]
save @m.x1.x1.x1.xm19.msky130_fd_pr__pfet_01v8_lvt[gm]
save @m.x1.x1.x1.xm20.msky130_fd_pr__nfet_01v8_lvt[gm]
save @m.x1.x1.x1.xm21.msky130_fd_pr__nfet_01v8_lvt[gm]
save @m.x1.x1.x1.xm22.msky130_fd_pr__pfet_01v8_lvt[gm]

save @m.x1.x1.x1.x1.xm1.msky130_fd_pr__pfet_01v8_lvt[gm]
save @m.x1.x1.x1.x1.xm2.msky130_fd_pr__nfet_01v8_lvt[gm]
save @m.x1.x1.x1.x1.xm3.msky130_fd_pr__pfet_01v8_lvt[gm]
save @m.x1.x1.x1.x1.xm4.msky130_fd_pr__nfet_01v8_lvt[gm]
save @m.x1.x1.x1.x1.xm5.msky130_fd_pr__nfet_01v8_lvt[gm]
save @m.x1.x1.x1.x1.xm6.msky130_fd_pr__nfet_01v8_lvt[gm]
save @m.x1.x1.x1.x1.xm7.msky130_fd_pr__pfet_01v8_lvt[gm]
save @m.x1.x1.x1.x1.xm8.msky130_fd_pr__pfet_01v8_lvt[gm]
save @m.x1.x1.x1.x1.xm9.msky130_fd_pr__nfet_01v8_lvt[gm]
save @m.x1.x1.x1.x1.xm10.msky130_fd_pr__nfet_01v8_lvt[gm]
save @m.x1.x1.x1.x1.xm11.msky130_fd_pr__pfet_01v8_lvt[gm]

save @m.x1.xm1.msky130_fd_pr__nfet_01v8_lvt[gm]
save @m.x1.xm2.msky130_fd_pr__nfet_01v8_lvt[gm]
save @m.x1.xm3.msky130_fd_pr__nfet_01v8_lvt[gm]
save @m.x1.xm4.msky130_fd_pr__nfet_01v8_lvt[gm]


save @m.x1.x1.x2.x1.xm5.msky130_fd_pr__nfet_01v8_lvt[vth]
save @m.x1.x1.x2.x1.xm1.msky130_fd_pr__nfet_01v8_lvt[vth]
save @m.x1.x1.x2.x1.xm2.msky130_fd_pr__nfet_01v8_lvt[vth]
save @m.x1.x1.x2.x1.xm3.msky130_fd_pr__nfet_01v8_lvt[vth]
save @m.x1.x1.x2.x1.xm4.msky130_fd_pr__nfet_01v8_lvt[vth]
save @m.x1.x1.x2.x1.xm6.msky130_fd_pr__nfet_01v8_lvt[vth]
save @m.x1.x1.x2.x1.xm7.msky130_fd_pr__nfet_01v8_lvt[vth]
save @m.x1.x1.x2.x1.xm8.msky130_fd_pr__nfet_01v8_lvt[vth]
save @m.x1.x1.x2.x1.xm9.msky130_fd_pr__nfet_01v8_lvt[vth]
save @m.x1.x1.x2.x1.xm10.msky130_fd_pr__nfet_01v8_lvt[vth]
save @m.x1.x1.x2.x1.xm11.msky130_fd_pr__pfet_01v8_lvt[vth]
save @m.x1.x1.x2.x1.xm12.msky130_fd_pr__pfet_01v8_lvt[vth]
save @m.x1.x1.x2.x1.xm13.msky130_fd_pr__pfet_01v8_lvt[vth]
save @m.x1.x1.x2.x1.xm14.msky130_fd_pr__pfet_01v8_lvt[vth]
save @m.x1.x1.x2.x1.xm15.msky130_fd_pr__nfet_01v8_lvt[vth]
save @m.x1.x1.x2.x1.xm16.msky130_fd_pr__nfet_01v8_lvt[vth]
save @m.x1.x1.x2.x1.xm17.msky130_fd_pr__nfet_01v8_lvt[vth]
save @m.x1.x1.x2.x1.xm18.msky130_fd_pr__nfet_01v8_lvt[vth]
save @m.x1.x1.x2.x1.xm19.msky130_fd_pr__nfet_01v8_lvt[vth]
save @m.x1.x1.x2.x1.xm20.msky130_fd_pr__pfet_01v8_lvt[vth]
save @m.x1.x1.x2.x1.xm21.msky130_fd_pr__pfet_01v8_lvt[vth]
save @m.x1.x1.x2.x1.xm22.msky130_fd_pr__nfet_01v8_lvt[vth]

save @m.x1.x1.x2.x2.xm1.msky130_fd_pr__nfet_01v8_lvt[vth]
save @m.x1.x1.x2.x2.xm2.msky130_fd_pr__nfet_01v8_lvt[vth]
save @m.x1.x1.x2.x2.xm3.msky130_fd_pr__pfet_01v8_lvt[vth]
save @m.x1.x1.x2.x2.xm4.msky130_fd_pr__pfet_01v8_lvt[vth]
save @m.x1.x1.x2.x2.xm5.msky130_fd_pr__nfet_01v8_lvt[vth]
save @m.x1.x1.x2.x2.xm6.msky130_fd_pr__nfet_01v8_lvt[vth]
save @m.x1.x1.x2.x2.xm7.msky130_fd_pr__pfet_01v8_lvt[vth]
save @m.x1.x1.x2.x2.xm8.msky130_fd_pr__pfet_01v8_lvt[vth]
save @m.x1.x1.x2.x2.xm9.msky130_fd_pr__pfet_01v8_lvt[vth]

save @m.x1.x1.x1.xm5.msky130_fd_pr__pfet_01v8_lvt[vth]
save @m.x1.x1.x1.xm1.msky130_fd_pr__pfet_01v8_lvt[vth]
save @m.x1.x1.x1.xm2.msky130_fd_pr__nfet_01v8_lvt[vth]
save @m.x1.x1.x1.xm3.msky130_fd_pr__nfet_01v8_lvt[vth]
save @m.x1.x1.x1.xm4.msky130_fd_pr__nfet_01v8_lvt[vth]
save @m.x1.x1.x1.xm6.msky130_fd_pr__pfet_01v8_lvt[vth]
save @m.x1.x1.x1.xm7.msky130_fd_pr__pfet_01v8_lvt[vth]
save @m.x1.x1.x1.xm8.msky130_fd_pr__pfet_01v8_lvt[vth]
save @m.x1.x1.x1.xm9.msky130_fd_pr__nfet_01v8_lvt[vth]
save @m.x1.x1.x1.xm10.msky130_fd_pr__nfet_01v8_lvt[vth]
save @m.x1.x1.x1.xm11.msky130_fd_pr__pfet_01v8_lvt[vth]
save @m.x1.x1.x1.xm12.msky130_fd_pr__nfet_01v8_lvt[vth]
save @m.x1.x1.x1.xm13.msky130_fd_pr__nfet_01v8_lvt[vth]
save @m.x1.x1.x1.xm14.msky130_fd_pr__nfet_01v8_lvt[vth]
save @m.x1.x1.x1.xm15.msky130_fd_pr__nfet_01v8_lvt[vth]
save @m.x1.x1.x1.xm16.msky130_fd_pr__pfet_01v8_lvt[vth]
save @m.x1.x1.x1.xm17.msky130_fd_pr__pfet_01v8_lvt[vth]
save @m.x1.x1.x1.xm18.msky130_fd_pr__pfet_01v8_lvt[vth]
save @m.x1.x1.x1.xm19.msky130_fd_pr__pfet_01v8_lvt[vth]
save @m.x1.x1.x1.xm20.msky130_fd_pr__nfet_01v8_lvt[vth]
save @m.x1.x1.x1.xm21.msky130_fd_pr__nfet_01v8_lvt[vth]
save @m.x1.x1.x1.xm22.msky130_fd_pr__nfet_01v8_lvt[vth]

save @m.x1.x1.x1.x1.xm1.msky130_fd_pr__pfet_01v8_lvt[vth]
save @m.x1.x1.x1.x1.xm2.msky130_fd_pr__nfet_01v8_lvt[vth]
save @m.x1.x1.x1.x1.xm3.msky130_fd_pr__pfet_01v8_lvt[vth]
save @m.x1.x1.x1.x1.xm4.msky130_fd_pr__nfet_01v8_lvt[vth]
save @m.x1.x1.x1.x1.xm5.msky130_fd_pr__nfet_01v8_lvt[vth]
save @m.x1.x1.x1.x1.xm6.msky130_fd_pr__nfet_01v8_lvt[vth]
save @m.x1.x1.x1.x1.xm7.msky130_fd_pr__pfet_01v8_lvt[vth]
save @m.x1.x1.x1.x1.xm8.msky130_fd_pr__pfet_01v8_lvt[vth]
save @m.x1.x1.x1.x1.xm9.msky130_fd_pr__nfet_01v8_lvt[vth]
save @m.x1.x1.x1.x1.xm10.msky130_fd_pr__nfet_01v8_lvt[vth]
save @m.x1.x1.x1.x1.xm11.msky130_fd_pr__pfet_01v8_lvt[vth]

save @m.x1.xm1.msky130_fd_pr__nfet_01v8_lvt[vth]
save @m.x1.xm2.msky130_fd_pr__nfet_01v8_lvt[vth]
save @m.x1.xm3.msky130_fd_pr__nfet_01v8_lvt[vth]
save @m.x1.xm4.msky130_fd_pr__nfet_01v8_lvt[vth]

op
*ac dec 101 1 10000MEG
*tran 100u 100m

dc Vy -0.1 0.1 0.05 Vx -0.1 0.1 0.05

let vdiff = v(Vop)-v(Vom)
*let vin = v(Vp) - v(Vm)
*plot db(vdiff/vin) (180/pi)*phase(vdiff/vin)
plot   vdiff
write Multiplier_tb.raw
.endc



**** end user architecture code
.end
